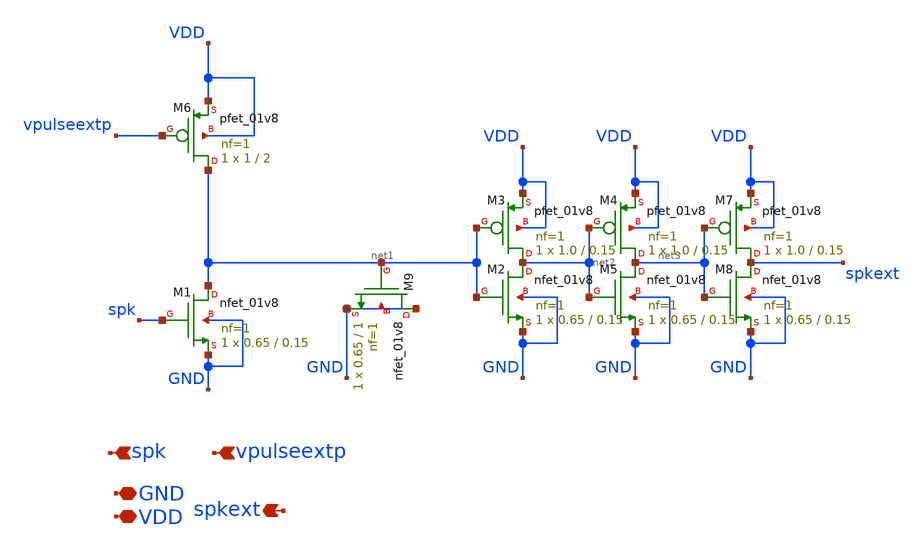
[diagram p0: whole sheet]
** sch_path: design/xschem/spike_extender.sch
**.subckt spike_extender GND VDD spk spkext vpulseextp
*.iopin GND
*.iopin VDD
*.ipin spk
*.opin spkext
*.ipin vpulseextp
XM1 net1 spk GND GND sky130_fd_pr__nfet_01v8 L=0.15 W=0.65 nf=1 ad='int((nf+1)/2) * W/nf * 0.29' as='int((nf+2)/2) * W/nf * 0.29'
+ pd='2*int((nf+1)/2) * (W/nf + 0.29)' ps='2*int((nf+2)/2) * (W/nf + 0.29)' nrd='0.29 / W' nrs='0.29 / W'
+ sa=0 sb=0 sd=0 mult=1 m=1
XM6 net1 vpulseextp VDD VDD sky130_fd_pr__pfet_01v8 L=2 W=1 nf=1 ad='int((nf+1)/2) * W/nf * 0.29' as='int((nf+2)/2) * W/nf * 0.29'
+ pd='2*int((nf+1)/2) * (W/nf + 0.29)' ps='2*int((nf+2)/2) * (W/nf + 0.29)' nrd='0.29 / W' nrs='0.29 / W'
+ sa=0 sb=0 sd=0 mult=1 m=1
XM5 net3 net2 GND GND sky130_fd_pr__nfet_01v8 L=0.15 W=0.65 nf=1 ad='int((nf+1)/2) * W/nf * 0.29' as='int((nf+2)/2) * W/nf * 0.29'
+ pd='2*int((nf+1)/2) * (W/nf + 0.29)' ps='2*int((nf+2)/2) * (W/nf + 0.29)' nrd='0.29 / W' nrs='0.29 / W'
+ sa=0 sb=0 sd=0 mult=1 m=1
XM8 spkext net3 GND GND sky130_fd_pr__nfet_01v8 L=0.15 W=0.65 nf=1 ad='int((nf+1)/2) * W/nf * 0.29' as='int((nf+2)/2) * W/nf * 0.29'
+ pd='2*int((nf+1)/2) * (W/nf + 0.29)' ps='2*int((nf+2)/2) * (W/nf + 0.29)' nrd='0.29 / W' nrs='0.29 / W'
+ sa=0 sb=0 sd=0 mult=1 m=1
XM4 net3 net2 VDD VDD sky130_fd_pr__pfet_01v8 L=0.15 W=1.0 nf=1 ad='int((nf+1)/2) * W/nf * 0.29' as='int((nf+2)/2) * W/nf * 0.29'
+ pd='2*int((nf+1)/2) * (W/nf + 0.29)' ps='2*int((nf+2)/2) * (W/nf + 0.29)' nrd='0.29 / W' nrs='0.29 / W'
+ sa=0 sb=0 sd=0 mult=1 m=1
XM7 spkext net3 VDD VDD sky130_fd_pr__pfet_01v8 L=0.15 W=1.0 nf=1 ad='int((nf+1)/2) * W/nf * 0.29' as='int((nf+2)/2) * W/nf * 0.29'
+ pd='2*int((nf+1)/2) * (W/nf + 0.29)' ps='2*int((nf+2)/2) * (W/nf + 0.29)' nrd='0.29 / W' nrs='0.29 / W'
+ sa=0 sb=0 sd=0 mult=1 m=1
XM2 net2 net1 GND GND sky130_fd_pr__nfet_01v8 L=0.15 W=0.65 nf=1 ad='int((nf+1)/2) * W/nf * 0.29' as='int((nf+2)/2) * W/nf * 0.29'
+ pd='2*int((nf+1)/2) * (W/nf + 0.29)' ps='2*int((nf+2)/2) * (W/nf + 0.29)' nrd='0.29 / W' nrs='0.29 / W'
+ sa=0 sb=0 sd=0 mult=1 m=1
XM3 net2 net1 VDD VDD sky130_fd_pr__pfet_01v8 L=0.15 W=1.0 nf=1 ad='int((nf+1)/2) * W/nf * 0.29' as='int((nf+2)/2) * W/nf * 0.29'
+ pd='2*int((nf+1)/2) * (W/nf + 0.29)' ps='2*int((nf+2)/2) * (W/nf + 0.29)' nrd='0.29 / W' nrs='0.29 / W'
+ sa=0 sb=0 sd=0 mult=1 m=1
XM9 GND net1 GND GND sky130_fd_pr__nfet_01v8 L=1 W=0.65 nf=1 ad='int((nf+1)/2) * W/nf * 0.29' as='int((nf+2)/2) * W/nf * 0.29'
+ pd='2*int((nf+1)/2) * (W/nf + 0.29)' ps='2*int((nf+2)/2) * (W/nf + 0.29)' nrd='0.29 / W' nrs='0.29 / W'
+ sa=0 sb=0 sd=0 mult=1 m=1
**.ends
.end
